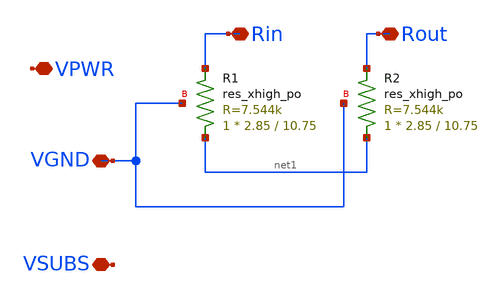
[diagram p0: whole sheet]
** sch_path: xschem/xschem/skywater_asc_res_xhigh_po_2p85_2.sch
**.subckt skywater_asc_res_xhigh_po_2p85_2 Rin Rout VPWR VGND VSUBS
*.iopin Rin
*.iopin Rout
*.iopin VPWR
*.iopin VGND
*.iopin VSUBS
XR1 net1 Rin VGND sky130_fd_pr__res_xhigh_po W=2.85 L=10.75 mult=1 m=1
XR2 net1 Rout VGND sky130_fd_pr__res_xhigh_po W=2.85 L=10.75 mult=1 m=1
**.ends
.end
